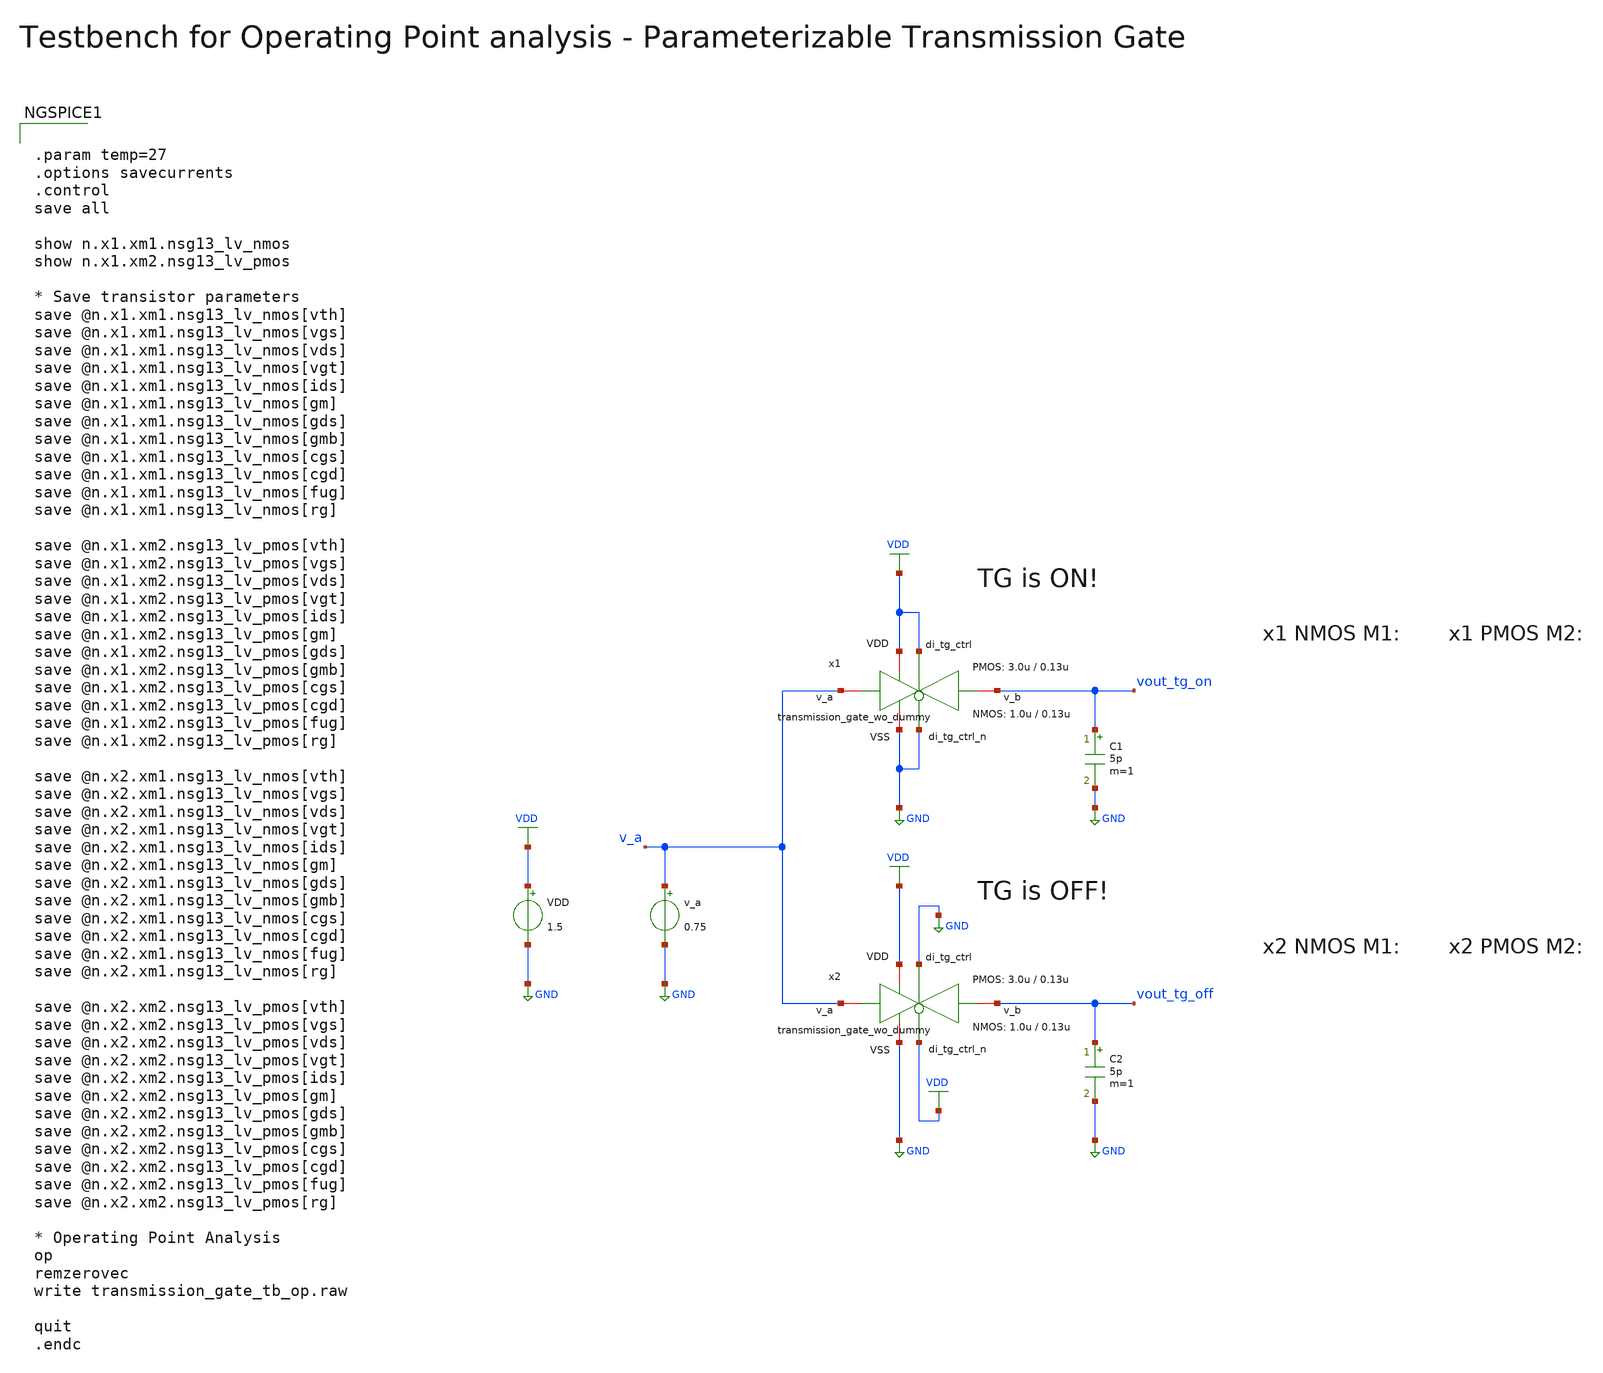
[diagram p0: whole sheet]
** sch_path: xschem/transmission_gate/testbenches/transmission_gate_tb_op.sch
**.subckt transmission_gate_tb_op
v_a v_a GND 0.75
VDD VDD GND 1.5
C1 vout_tg_on GND 5p m=1
C2 vout_tg_off GND 5p m=1
x1 VDD VDD GND vout_tg_on v_a GND transmission_gate_wo_dummy W_P=3.0u L_P=0.13u W_N=1.0u L_N=0.13u
x2 VDD GND GND vout_tg_off v_a VDD transmission_gate_wo_dummy W_P=3.0u L_P=0.13u W_N=1.0u L_N=0.13u
**** begin user architecture code

.lib cornerMOSlv.lib mos_tt
.lib cornerRES.lib res_typ



.param temp=27
.options savecurrents
.control
save all

show n.x1.xm1.nsg13_lv_nmos
show n.x1.xm2.nsg13_lv_pmos

* Save transistor parameters
save @n.x1.xm1.nsg13_lv_nmos[vth]
save @n.x1.xm1.nsg13_lv_nmos[vgs]
save @n.x1.xm1.nsg13_lv_nmos[vds]
save @n.x1.xm1.nsg13_lv_nmos[vgt]
save @n.x1.xm1.nsg13_lv_nmos[ids]
save @n.x1.xm1.nsg13_lv_nmos[gm]
save @n.x1.xm1.nsg13_lv_nmos[gds]
save @n.x1.xm1.nsg13_lv_nmos[gmb]
save @n.x1.xm1.nsg13_lv_nmos[cgs]
save @n.x1.xm1.nsg13_lv_nmos[cgd]
save @n.x1.xm1.nsg13_lv_nmos[fug]
save @n.x1.xm1.nsg13_lv_nmos[rg]

save @n.x1.xm2.nsg13_lv_pmos[vth]
save @n.x1.xm2.nsg13_lv_pmos[vgs]
save @n.x1.xm2.nsg13_lv_pmos[vds]
save @n.x1.xm2.nsg13_lv_pmos[vgt]
save @n.x1.xm2.nsg13_lv_pmos[ids]
save @n.x1.xm2.nsg13_lv_pmos[gm]
save @n.x1.xm2.nsg13_lv_pmos[gds]
save @n.x1.xm2.nsg13_lv_pmos[gmb]
save @n.x1.xm2.nsg13_lv_pmos[cgs]
save @n.x1.xm2.nsg13_lv_pmos[cgd]
save @n.x1.xm2.nsg13_lv_pmos[fug]
save @n.x1.xm2.nsg13_lv_pmos[rg]

save @n.x2.xm1.nsg13_lv_nmos[vth]
save @n.x2.xm1.nsg13_lv_nmos[vgs]
save @n.x2.xm1.nsg13_lv_nmos[vds]
save @n.x2.xm1.nsg13_lv_nmos[vgt]
save @n.x2.xm1.nsg13_lv_nmos[ids]
save @n.x2.xm1.nsg13_lv_nmos[gm]
save @n.x2.xm1.nsg13_lv_nmos[gds]
save @n.x2.xm1.nsg13_lv_nmos[gmb]
save @n.x2.xm1.nsg13_lv_nmos[cgs]
save @n.x2.xm1.nsg13_lv_nmos[cgd]
save @n.x2.xm1.nsg13_lv_nmos[fug]
save @n.x2.xm1.nsg13_lv_nmos[rg]

save @n.x2.xm2.nsg13_lv_pmos[vth]
save @n.x2.xm2.nsg13_lv_pmos[vgs]
save @n.x2.xm2.nsg13_lv_pmos[vds]
save @n.x2.xm2.nsg13_lv_pmos[vgt]
save @n.x2.xm2.nsg13_lv_pmos[ids]
save @n.x2.xm2.nsg13_lv_pmos[gm]
save @n.x2.xm2.nsg13_lv_pmos[gds]
save @n.x2.xm2.nsg13_lv_pmos[gmb]
save @n.x2.xm2.nsg13_lv_pmos[cgs]
save @n.x2.xm2.nsg13_lv_pmos[cgd]
save @n.x2.xm2.nsg13_lv_pmos[fug]
save @n.x2.xm2.nsg13_lv_pmos[rg]

* Operating Point Analysis
op
remzerovec
write transmission_gate_tb_op.raw

quit
.endc

**** end user architecture code
**.ends

* expanding   symbol:  transmission_gate/transmission_gate_wo_dummy.sym # of pins=6
** sym_path: xschem/transmission_gate/transmission_gate_wo_dummy.sym
** sch_path: xschem/transmission_gate/transmission_gate_wo_dummy.sch
.subckt transmission_gate_wo_dummy VDD di_tg_ctrl VSS v_b v_a di_tg_ctrl_n  W_P=3.0u L_P=0.13u
+ W_N=1.0u L_N=0.13u
*.iopin v_a
*.iopin v_b
*.iopin VDD
*.iopin VSS
*.ipin di_tg_ctrl
*.ipin di_tg_ctrl_n
XM1 v_b di_tg_ctrl v_a VSS sg13_lv_nmos w=W_N l=L_N ng=1 m=1 mm_ok=1
XM2 v_a di_tg_ctrl_n v_b VDD sg13_lv_pmos w=W_P l=L_P ng=1 m=1 mm_ok=1
.ends

.GLOBAL GND
.GLOBAL VDD
.end
